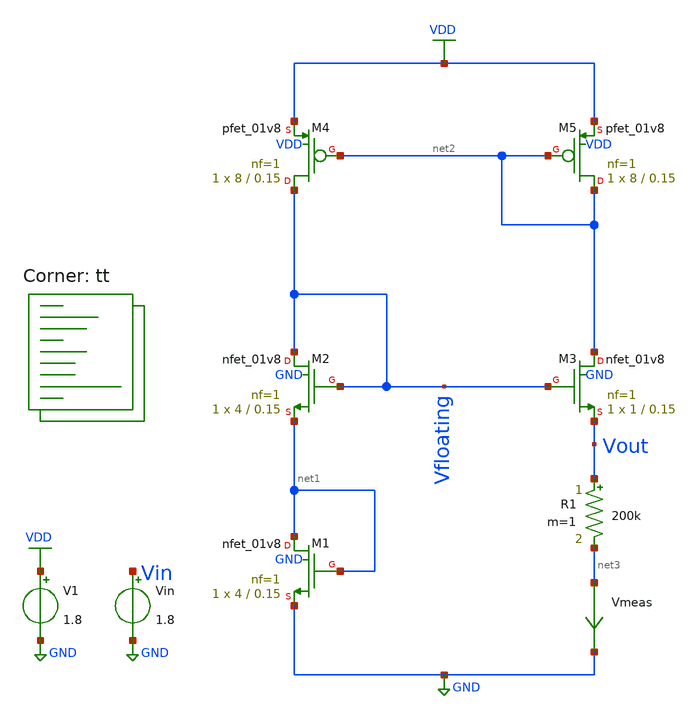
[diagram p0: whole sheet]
** sch_path: projects/pll/bandgapref/xschem_ngspice/mos_bandgap1.sch
**.subckt mos_bandgap1
XM1 net1 net1 GND GND sky130_fd_pr__nfet_01v8 L=0.15 W=4 nf=1 ad='int((nf+1)/2) * W/nf * 0.29' as='int((nf+2)/2) * W/nf * 0.29'
+ pd='2*int((nf+1)/2) * (W/nf + 0.29)' ps='2*int((nf+2)/2) * (W/nf + 0.29)' nrd='0.29 / W' nrs='0.29 / W'
+ sa=0 sb=0 sd=0 mult=1 m=1
XM2 Vfloating Vfloating net1 GND sky130_fd_pr__nfet_01v8 L=0.15 W=4 nf=1 ad='int((nf+1)/2) * W/nf * 0.29'
+ as='int((nf+2)/2) * W/nf * 0.29' pd='2*int((nf+1)/2) * (W/nf + 0.29)' ps='2*int((nf+2)/2) * (W/nf + 0.29)'
+ nrd='0.29 / W' nrs='0.29 / W' sa=0 sb=0 sd=0 mult=1 m=1
XM3 net2 Vfloating Vout GND sky130_fd_pr__nfet_01v8 L=0.15 W=1 nf=1 ad='int((nf+1)/2) * W/nf * 0.29'
+ as='int((nf+2)/2) * W/nf * 0.29' pd='2*int((nf+1)/2) * (W/nf + 0.29)' ps='2*int((nf+2)/2) * (W/nf + 0.29)'
+ nrd='0.29 / W' nrs='0.29 / W' sa=0 sb=0 sd=0 mult=1 m=1
XM4 Vfloating net2 VDD VDD sky130_fd_pr__pfet_01v8 L=0.15 W=8 nf=1 ad='int((nf+1)/2) * W/nf * 0.29' as='int((nf+2)/2) * W/nf * 0.29'
+ pd='2*int((nf+1)/2) * (W/nf + 0.29)' ps='2*int((nf+2)/2) * (W/nf + 0.29)' nrd='0.29 / W' nrs='0.29 / W'
+ sa=0 sb=0 sd=0 mult=1 m=1
XM5 net2 net2 VDD VDD sky130_fd_pr__pfet_01v8 L=0.15 W=8 nf=1 ad='int((nf+1)/2) * W/nf * 0.29' as='int((nf+2)/2) * W/nf * 0.29'
+ pd='2*int((nf+1)/2) * (W/nf + 0.29)' ps='2*int((nf+2)/2) * (W/nf + 0.29)' nrd='0.29 / W' nrs='0.29 / W'
+ sa=0 sb=0 sd=0 mult=1 m=1
V1 VDD GND 1.8
R1 Vout net3 200k m=1
Vin Vin GND 1.8
Vmeas net3 GND 0
.save i(vmeas)
**** begin user architecture code
.lib $::SKYWATER_MODELS/sky130.lib.spice tt



.option wnflag=1

.control

  save all
  dc Vin 0 1.8 0.1
  write mos_bandgap1.raw
  set appendwrite

.endc



**** end user architecture code
**.ends
.GLOBAL GND
.GLOBAL VDD
.end
